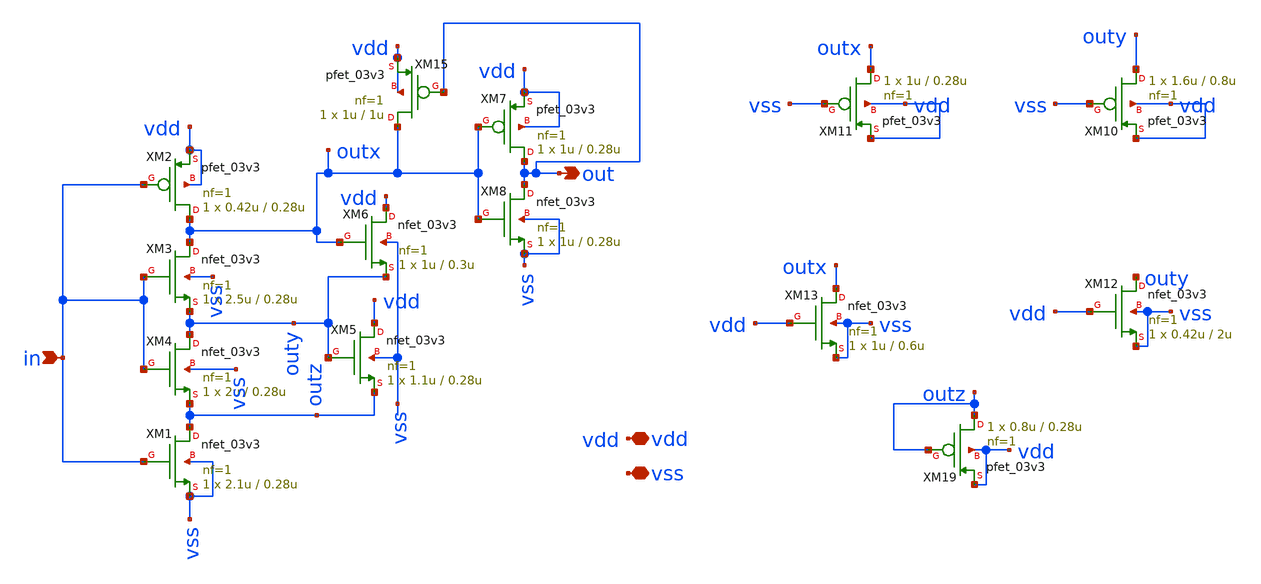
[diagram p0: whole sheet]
** sch_path: designs/libs/core_schmitt_trigger/schmitt_trigger.sch
**.subckt schmitt_trigger in out vdd vss
*.ipin in
*.opin out
*.iopin vdd
*.iopin vss
XM2 outx in vdd vdd pfet_03v3 L=0.28u W=0.42u nf=1 ad='int((nf+1)/2) * W/nf * 0.18u' as='int((nf+2)/2) * W/nf * 0.18u'
+ pd='2*int((nf+1)/2) * (W/nf + 0.18u)' ps='2*int((nf+2)/2) * (W/nf + 0.18u)' nrd='0.18u / W' nrs='0.18u / W'
+ sa=0 sb=0 sd=0 m=1
XM1 outz in vss vss nfet_03v3 L=0.28u W=2.1u nf=1 ad='int((nf+1)/2) * W/nf * 0.18u' as='int((nf+2)/2) * W/nf * 0.18u'
+ pd='2*int((nf+1)/2) * (W/nf + 0.18u)' ps='2*int((nf+2)/2) * (W/nf + 0.18u)' nrd='0.18u / W' nrs='0.18u / W'
+ sa=0 sb=0 sd=0 m=1
XM4 outy in outz vss nfet_03v3 L=0.28u W=2u nf=1 ad='int((nf+1)/2) * W/nf * 0.18u' as='int((nf+2)/2) * W/nf * 0.18u'
+ pd='2*int((nf+1)/2) * (W/nf + 0.18u)' ps='2*int((nf+2)/2) * (W/nf + 0.18u)' nrd='0.18u / W' nrs='0.18u / W'
+ sa=0 sb=0 sd=0 m=1
XM3 outx in outy vss nfet_03v3 L=0.28u W=2.5u nf=1 ad='int((nf+1)/2) * W/nf * 0.18u' as='int((nf+2)/2) * W/nf * 0.18u'
+ pd='2*int((nf+1)/2) * (W/nf + 0.18u)' ps='2*int((nf+2)/2) * (W/nf + 0.18u)' nrd='0.18u / W' nrs='0.18u / W'
+ sa=0 sb=0 sd=0 m=1
XM5 vdd outy outz vss nfet_03v3 L=0.28u W=1.1u nf=1 ad='int((nf+1)/2) * W/nf * 0.18u' as='int((nf+2)/2) * W/nf * 0.18u'
+ pd='2*int((nf+1)/2) * (W/nf + 0.18u)' ps='2*int((nf+2)/2) * (W/nf + 0.18u)' nrd='0.18u / W' nrs='0.18u / W'
+ sa=0 sb=0 sd=0 m=1
XM6 vdd outx outy vss nfet_03v3 L=0.3u W=1u nf=1 ad='int((nf+1)/2) * W/nf * 0.18u' as='int((nf+2)/2) * W/nf * 0.18u'
+ pd='2*int((nf+1)/2) * (W/nf + 0.18u)' ps='2*int((nf+2)/2) * (W/nf + 0.18u)' nrd='0.18u / W' nrs='0.18u / W'
+ sa=0 sb=0 sd=0 m=1
XM8 out outx vss vss nfet_03v3 L=0.28u W=1u nf=1 ad='int((nf+1)/2) * W/nf * 0.18u' as='int((nf+2)/2) * W/nf * 0.18u'
+ pd='2*int((nf+1)/2) * (W/nf + 0.18u)' ps='2*int((nf+2)/2) * (W/nf + 0.18u)' nrd='0.18u / W' nrs='0.18u / W'
+ sa=0 sb=0 sd=0 m=1
XM7 out outx vdd vdd pfet_03v3 L=0.28u W=1u nf=1 ad='int((nf+1)/2) * W/nf * 0.18u' as='int((nf+2)/2) * W/nf * 0.18u'
+ pd='2*int((nf+1)/2) * (W/nf + 0.18u)' ps='2*int((nf+2)/2) * (W/nf + 0.18u)' nrd='0.18u / W' nrs='0.18u / W'
+ sa=0 sb=0 sd=0 m=1
XM10 outy vss vdd vdd pfet_03v3 L=0.8u W=1.6u nf=1 ad='int((nf+1)/2) * W/nf * 0.18u' as='int((nf+2)/2) * W/nf * 0.18u'
+ pd='2*int((nf+1)/2) * (W/nf + 0.18u)' ps='2*int((nf+2)/2) * (W/nf + 0.18u)' nrd='0.18u / W' nrs='0.18u / W'
+ sa=0 sb=0 sd=0 m=1
XM11 outx vss vdd vdd pfet_03v3 L=0.28u W=1u nf=1 ad='int((nf+1)/2) * W/nf * 0.18u' as='int((nf+2)/2) * W/nf * 0.18u'
+ pd='2*int((nf+1)/2) * (W/nf + 0.18u)' ps='2*int((nf+2)/2) * (W/nf + 0.18u)' nrd='0.18u / W' nrs='0.18u / W'
+ sa=0 sb=0 sd=0 m=1
XM12 outy vdd vss vss nfet_03v3 L=2u W=0.42u nf=1 ad='int((nf+1)/2) * W/nf * 0.18u' as='int((nf+2)/2) * W/nf * 0.18u'
+ pd='2*int((nf+1)/2) * (W/nf + 0.18u)' ps='2*int((nf+2)/2) * (W/nf + 0.18u)' nrd='0.18u / W' nrs='0.18u / W'
+ sa=0 sb=0 sd=0 m=1
XM13 outx vdd vss vss nfet_03v3 L=0.6u W=1u nf=1 ad='int((nf+1)/2) * W/nf * 0.18u' as='int((nf+2)/2) * W/nf * 0.18u'
+ pd='2*int((nf+1)/2) * (W/nf + 0.18u)' ps='2*int((nf+2)/2) * (W/nf + 0.18u)' nrd='0.18u / W' nrs='0.18u / W'
+ sa=0 sb=0 sd=0 m=1
XM19 outz outz vdd vdd pfet_03v3 L=0.28u W=0.8u nf=1 ad='int((nf+1)/2) * W/nf * 0.18u' as='int((nf+2)/2) * W/nf * 0.18u'
+ pd='2*int((nf+1)/2) * (W/nf + 0.18u)' ps='2*int((nf+2)/2) * (W/nf + 0.18u)' nrd='0.18u / W' nrs='0.18u / W'
+ sa=0 sb=0 sd=0 m=1
XM15 outx out vdd vdd pfet_03v3 L=1u W=1u nf=1 ad='int((nf+1)/2) * W/nf * 0.18u' as='int((nf+2)/2) * W/nf * 0.18u'
+ pd='2*int((nf+1)/2) * (W/nf + 0.18u)' ps='2*int((nf+2)/2) * (W/nf + 0.18u)' nrd='0.18u / W' nrs='0.18u / W'
+ sa=0 sb=0 sd=0 m=1
**.ends
.end
